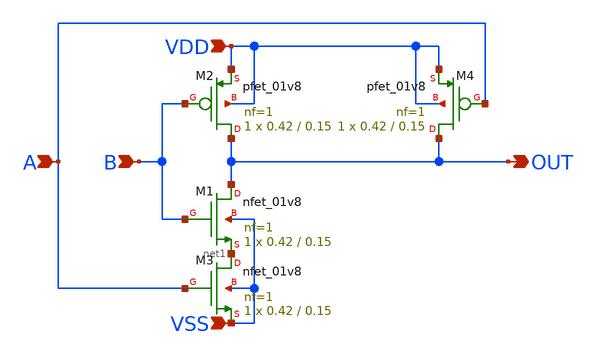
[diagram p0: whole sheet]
** sch_path: xschem/hgu_nand.sch
**.subckt hgu_nand B OUT A VDD VSS
*.ipin B
*.opin OUT
*.ipin A
*.ipin VDD
*.ipin VSS
XM2 OUT B VDD VDD sky130_fd_pr__pfet_01v8 L=0.15 W=0.42 nf=1 ad='int((nf+1)/2) * W/nf * 0.29' as='int((nf+2)/2) * W/nf * 0.29'
+ pd='2*int((nf+1)/2) * (W/nf + 0.29)' ps='2*int((nf+2)/2) * (W/nf + 0.29)' nrd='0.29 / W' nrs='0.29 / W'
+ sa=0 sb=0 sd=0 mult=1 m=1
XM1 OUT B net1 VSS sky130_fd_pr__nfet_01v8 L=0.15 W=0.42 nf=1 ad='int((nf+1)/2) * W/nf * 0.29' as='int((nf+2)/2) * W/nf * 0.29'
+ pd='2*int((nf+1)/2) * (W/nf + 0.29)' ps='2*int((nf+2)/2) * (W/nf + 0.29)' nrd='0.29 / W' nrs='0.29 / W'
+ sa=0 sb=0 sd=0 mult=1 m=1
XM3 net1 A VSS VSS sky130_fd_pr__nfet_01v8 L=0.15 W=0.42 nf=1 ad='int((nf+1)/2) * W/nf * 0.29' as='int((nf+2)/2) * W/nf * 0.29'
+ pd='2*int((nf+1)/2) * (W/nf + 0.29)' ps='2*int((nf+2)/2) * (W/nf + 0.29)' nrd='0.29 / W' nrs='0.29 / W'
+ sa=0 sb=0 sd=0 mult=1 m=1
XM4 OUT A VDD VDD sky130_fd_pr__pfet_01v8 L=0.15 W=0.42 nf=1 ad='int((nf+1)/2) * W/nf * 0.29' as='int((nf+2)/2) * W/nf * 0.29'
+ pd='2*int((nf+1)/2) * (W/nf + 0.29)' ps='2*int((nf+2)/2) * (W/nf + 0.29)' nrd='0.29 / W' nrs='0.29 / W'
+ sa=0 sb=0 sd=0 mult=1 m=1
**.ends
.end
